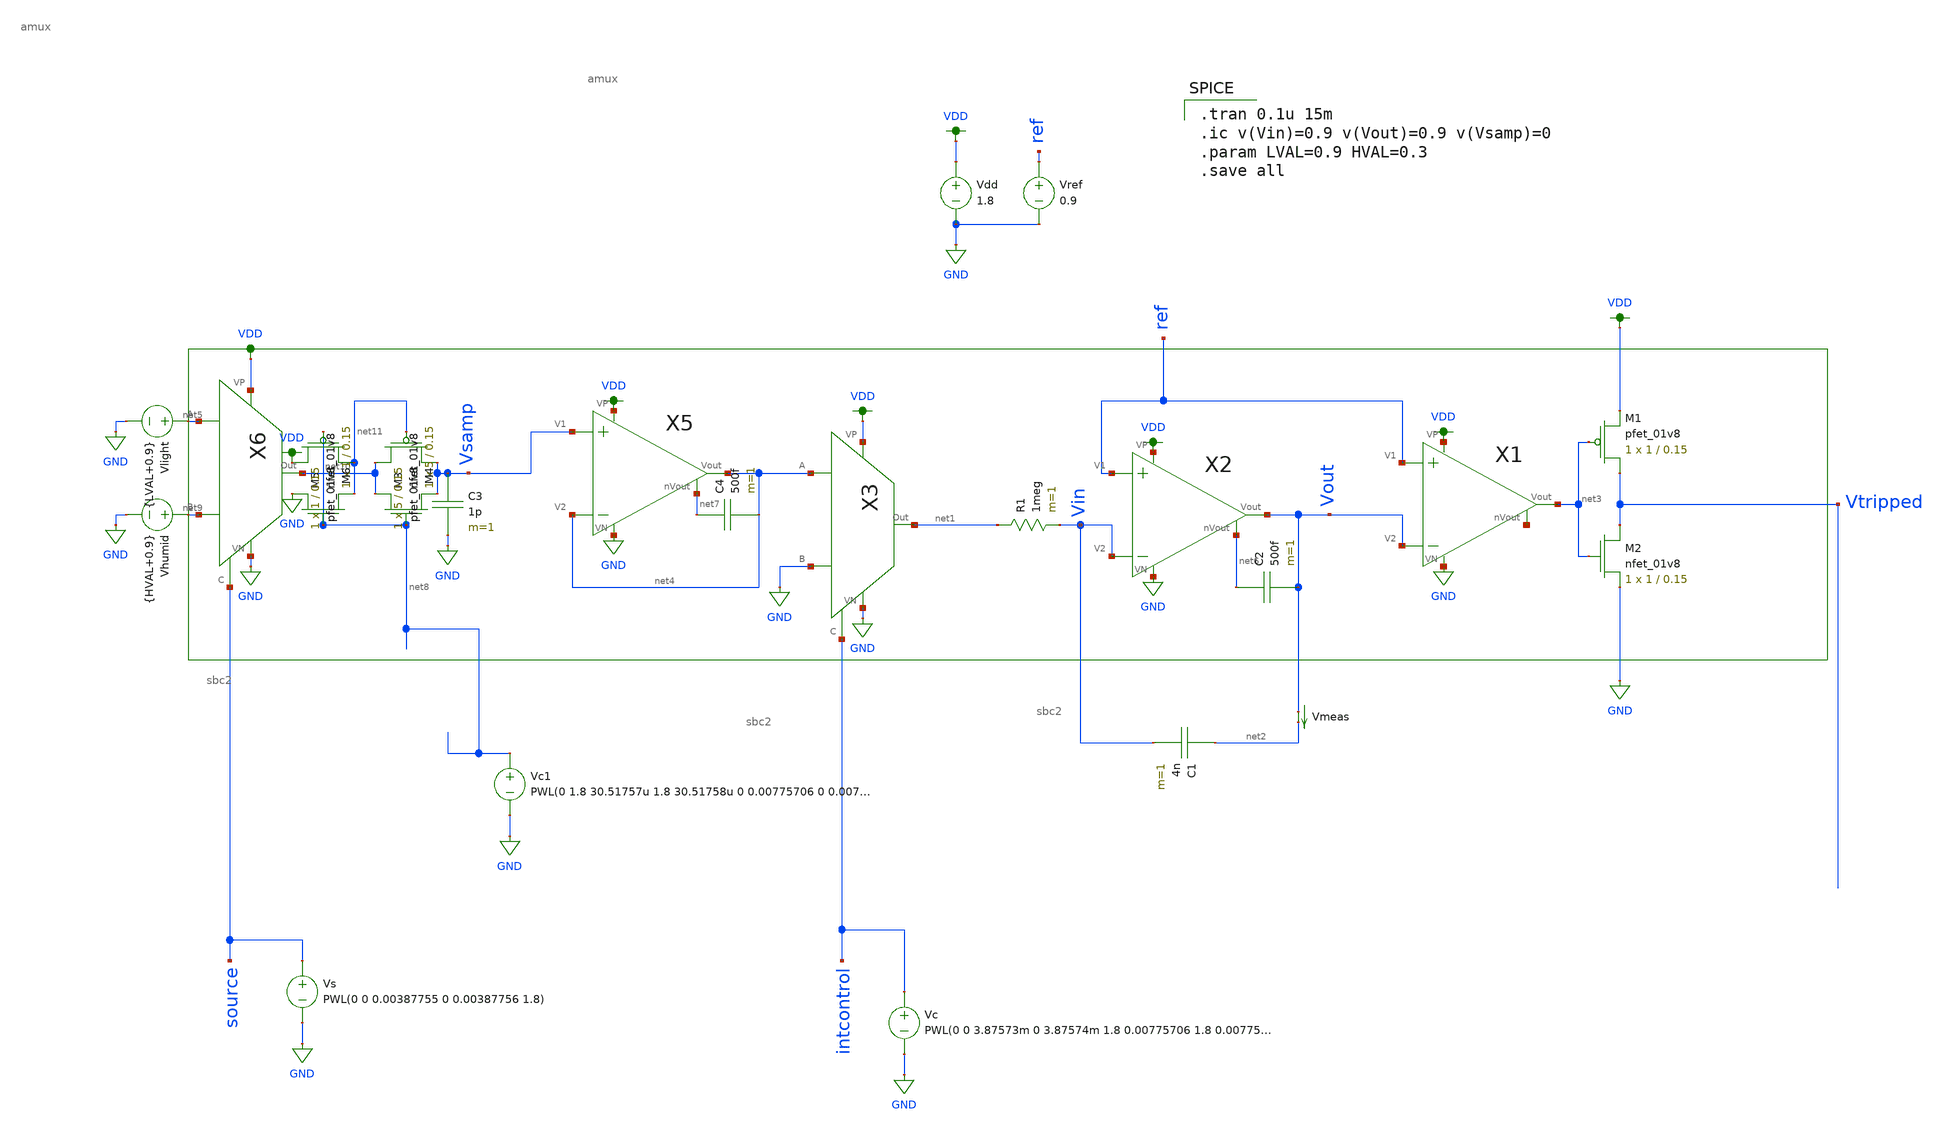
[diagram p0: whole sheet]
** sch_path: analog/adc_testing.sch
**.subckt adc_testing
Vdd VDD GND 1.8
C1 net2 Vin 4n m=1
R1 net1 Vin 1meg m=1
Vlight net5 GND {LVAL+0.9}
Vref ref GND 0.9
Vmeas Vout net2 0
.save i(vmeas)
XM1 Vtripped net3 VDD VDD sky130_fd_pr__pfet_01v8 L=0.15 W=1 nf=1 ad='int((nf+1)/2) * W/nf * 0.29' as='int((nf+2)/2) * W/nf * 0.29'
+ pd='2*int((nf+1)/2) * (W/nf + 0.29)' ps='2*int((nf+2)/2) * (W/nf + 0.29)' nrd='0.29 / W' nrs='0.29 / W'
+ sa=0 sb=0 sd=0 mult=1 m=1
XM2 Vtripped net3 GND GND sky130_fd_pr__nfet_01v8 L=0.15 W=1 nf=1 ad='int((nf+1)/2) * W/nf * 0.29' as='int((nf+2)/2) * W/nf * 0.29'
+ pd='2*int((nf+1)/2) * (W/nf + 0.29)' ps='2*int((nf+2)/2) * (W/nf + 0.29)' nrd='0.29 / W' nrs='0.29 / W'
+ sa=0 sb=0 sd=0 mult=1 m=1
X3 net4 GND net1 VDD GND intcontrol amux
C2 net6 Vout 500f m=1
X1 ref Vout net12 net3 GND VDD sbc2
X2 ref Vin net6 Vout GND VDD sbc2
X5 Vsamp net4 net7 net4 GND VDD sbc2
C3 Vsamp GND 1p m=1
C4 net7 net4 500f m=1
XM3 net10 net8 Vsamp GND sky130_fd_pr__nfet_01v8 L=0.15 W=5 nf=1 ad='int((nf+1)/2) * W/nf * 0.29' as='int((nf+2)/2) * W/nf * 0.29'
+ pd='2*int((nf+1)/2) * (W/nf + 0.29)' ps='2*int((nf+2)/2) * (W/nf + 0.29)' nrd='0.29 / W' nrs='0.29 / W'
+ sa=0 sb=0 sd=0 mult=1 m=1
X6 net5 net9 net10 VDD GND source amux
Vhumid net9 GND {HVAL+0.9}
Vs source GND PWL(0 0 0.00387755 0 0.00387756 1.8)
Vc intcontrol GND PWL(0 0 3.87573m 0 3.87574m 1.8 0.00775706 1.8 0.007757061 0 0.01163461 0
+ 0.01163462 1.8)
XM4 net10 net11 Vsamp VDD sky130_fd_pr__pfet_01v8 L=0.15 W=5 nf=1 ad='int((nf+1)/2) * W/nf * 0.29' as='int((nf+2)/2) * W/nf * 0.29'
+ pd='2*int((nf+1)/2) * (W/nf + 0.29)' ps='2*int((nf+2)/2) * (W/nf + 0.29)' nrd='0.29 / W' nrs='0.29 / W'
+ sa=0 sb=0 sd=0 mult=1 m=1
Vc1 net8 GND PWL(0 1.8 30.51757u 1.8 30.51758u 0 0.00775706 0 0.007757061 1.8 0.00778757 1.8
+ 0.00778758 0)
XM5 GND net8 net11 GND sky130_fd_pr__nfet_01v8 L=0.15 W=1 nf=1 ad='int((nf+1)/2) * W/nf * 0.29' as='int((nf+2)/2) * W/nf * 0.29'
+ pd='2*int((nf+1)/2) * (W/nf + 0.29)' ps='2*int((nf+2)/2) * (W/nf + 0.29)' nrd='0.29 / W' nrs='0.29 / W'
+ sa=0 sb=0 sd=0 mult=1 m=1
XM6 VDD net8 net11 VDD sky130_fd_pr__pfet_01v8 L=0.15 W=1 nf=1 ad='int((nf+1)/2) * W/nf * 0.29' as='int((nf+2)/2) * W/nf * 0.29'
+ pd='2*int((nf+1)/2) * (W/nf + 0.29)' ps='2*int((nf+2)/2) * (W/nf + 0.29)' nrd='0.29 / W' nrs='0.29 / W'
+ sa=0 sb=0 sd=0 mult=1 m=1
**** begin user architecture code

.option wnflag=1
.param MC_SWITCH=0.0
.lib ~/skywater/skywater-pdk/libraries/sky130_fd_pr_ngspice/latest/models/sky130.lib.spice tt


.tran 0.1u 15m
.ic v(Vin)=0.9 v(Vout)=0.9 v(Vsamp)=0
.param LVAL=0.9 HVAL=0.3
.save all

**** end user architecture code
**.ends

* expanding   symbol:  /home/jonah/VLSI/final/amux.sym # of pins=6
** sym_path: analog/amux.sym
** sch_path: analog/amux.sch
.subckt amux A B Out VP VN C
*.iopin VN
*.iopin VP
*.ipin C
*.ipin A
*.ipin B
*.opin Out
XM1 B net1 Out VDD sky130_fd_pr__pfet_01v8 L=0.15 W=1 nf=1 ad='int((nf+1)/2) * W/nf * 0.29' as='int((nf+2)/2) * W/nf * 0.29'
+ pd='2*int((nf+1)/2) * (W/nf + 0.29)' ps='2*int((nf+2)/2) * (W/nf + 0.29)' nrd='0.29 / W' nrs='0.29 / W'
+ sa=0 sb=0 sd=0 mult=1 m=1
XM2 Out C B GND sky130_fd_pr__nfet_01v8 L=0.15 W=1 nf=1 ad='int((nf+1)/2) * W/nf * 0.29' as='int((nf+2)/2) * W/nf * 0.29'
+ pd='2*int((nf+1)/2) * (W/nf + 0.29)' ps='2*int((nf+2)/2) * (W/nf + 0.29)' nrd='0.29 / W' nrs='0.29 / W'
+ sa=0 sb=0 sd=0 mult=1 m=1
XM3 Out C A VDD sky130_fd_pr__pfet_01v8 L=0.15 W=1 nf=1 ad='int((nf+1)/2) * W/nf * 0.29' as='int((nf+2)/2) * W/nf * 0.29'
+ pd='2*int((nf+1)/2) * (W/nf + 0.29)' ps='2*int((nf+2)/2) * (W/nf + 0.29)' nrd='0.29 / W' nrs='0.29 / W'
+ sa=0 sb=0 sd=0 mult=1 m=1
XM4 A net1 Out GND sky130_fd_pr__nfet_01v8 L=0.15 W=1 nf=1 ad='int((nf+1)/2) * W/nf * 0.29' as='int((nf+2)/2) * W/nf * 0.29'
+ pd='2*int((nf+1)/2) * (W/nf + 0.29)' ps='2*int((nf+2)/2) * (W/nf + 0.29)' nrd='0.29 / W' nrs='0.29 / W'
+ sa=0 sb=0 sd=0 mult=1 m=1
XM5 net1 C VP VDD sky130_fd_pr__pfet_01v8 L=0.15 W=1 nf=1 ad='int((nf+1)/2) * W/nf * 0.29' as='int((nf+2)/2) * W/nf * 0.29'
+ pd='2*int((nf+1)/2) * (W/nf + 0.29)' ps='2*int((nf+2)/2) * (W/nf + 0.29)' nrd='0.29 / W' nrs='0.29 / W'
+ sa=0 sb=0 sd=0 mult=1 m=1
XM6 VN C net1 GND sky130_fd_pr__nfet_01v8 L=0.15 W=1 nf=1 ad='int((nf+1)/2) * W/nf * 0.29' as='int((nf+2)/2) * W/nf * 0.29'
+ pd='2*int((nf+1)/2) * (W/nf + 0.29)' ps='2*int((nf+2)/2) * (W/nf + 0.29)' nrd='0.29 / W' nrs='0.29 / W'
+ sa=0 sb=0 sd=0 mult=1 m=1
.ends


* expanding   symbol:  /home/jonah/VLSI/final/sbc2.sym # of pins=6
** sym_path: analog/sbc2.sym
** sch_path: analog/sbc2.sch
.subckt sbc2 V1 V2 nVout Vout VN VP
*.ipin V1
*.ipin V2
*.iopin Vout
*.iopin nVout
*.iopin VP
*.iopin VN
XM7a net2 V1 net1 GND sky130_fd_pr__nfet_01v8 L=0.6 W=1.5 nf=1 ad='int((nf+1)/2) * W/nf * 0.29' as='int((nf+2)/2) * W/nf * 0.29'
+ pd='2*int((nf+1)/2) * (W/nf + 0.29)' ps='2*int((nf+2)/2) * (W/nf + 0.29)' nrd='0.29 / W' nrs='0.29 / W'
+ sa=0 sb=0 sd=0 mult=1 m=1
XM8a net3 V2 net2 GND sky130_fd_pr__nfet_01v8 L=0.6 W=1.5 nf=1 ad='int((nf+1)/2) * W/nf * 0.29' as='int((nf+2)/2) * W/nf * 0.29'
+ pd='2*int((nf+1)/2) * (W/nf + 0.29)' ps='2*int((nf+2)/2) * (W/nf + 0.29)' nrd='0.29 / W' nrs='0.29 / W'
+ sa=0 sb=0 sd=0 mult=1 m=1
XM8b net2 V2 net3 GND sky130_fd_pr__nfet_01v8 L=0.6 W=1.5 nf=1 ad='int((nf+1)/2) * W/nf * 0.29' as='int((nf+2)/2) * W/nf * 0.29'
+ pd='2*int((nf+1)/2) * (W/nf + 0.29)' ps='2*int((nf+2)/2) * (W/nf + 0.29)' nrd='0.29 / W' nrs='0.29 / W'
+ sa=0 sb=0 sd=0 mult=1 m=1
XM7b net1 V1 net2 GND sky130_fd_pr__nfet_01v8 L=0.6 W=1.5 nf=1 ad='int((nf+1)/2) * W/nf * 0.29' as='int((nf+2)/2) * W/nf * 0.29'
+ pd='2*int((nf+1)/2) * (W/nf + 0.29)' ps='2*int((nf+2)/2) * (W/nf + 0.29)' nrd='0.29 / W' nrs='0.29 / W'
+ sa=0 sb=0 sd=0 mult=1 m=1
XMd1 net1 VN VN GND sky130_fd_pr__nfet_01v8 L=0.6 W=1.5 nf=1 ad='int((nf+1)/2) * W/nf * 0.29' as='int((nf+2)/2) * W/nf * 0.29'
+ pd='2*int((nf+1)/2) * (W/nf + 0.29)' ps='2*int((nf+2)/2) * (W/nf + 0.29)' nrd='0.29 / W' nrs='0.29 / W'
+ sa=0 sb=0 sd=0 mult=1 m=1
XMd2 VN VN net1 GND sky130_fd_pr__nfet_01v8 L=0.6 W=1.5 nf=1 ad='int((nf+1)/2) * W/nf * 0.29' as='int((nf+2)/2) * W/nf * 0.29'
+ pd='2*int((nf+1)/2) * (W/nf + 0.29)' ps='2*int((nf+2)/2) * (W/nf + 0.29)' nrd='0.29 / W' nrs='0.29 / W'
+ sa=0 sb=0 sd=0 mult=1 m=1
XMd3 VP VP net4 VDD sky130_fd_pr__pfet_01v8 L=0.6 W=1.5 nf=1 ad='int((nf+1)/2) * W/nf * 0.29' as='int((nf+2)/2) * W/nf * 0.29'
+ pd='2*int((nf+1)/2) * (W/nf + 0.29)' ps='2*int((nf+2)/2) * (W/nf + 0.29)' nrd='0.29 / W' nrs='0.29 / W'
+ sa=0 sb=0 sd=0 mult=1 m=1
XM15a net4 V2 net5 VDD sky130_fd_pr__pfet_01v8 L=0.6 W=1.5 nf=1 ad='int((nf+1)/2) * W/nf * 0.29' as='int((nf+2)/2) * W/nf * 0.29'
+ pd='2*int((nf+1)/2) * (W/nf + 0.29)' ps='2*int((nf+2)/2) * (W/nf + 0.29)' nrd='0.29 / W' nrs='0.29 / W'
+ sa=0 sb=0 sd=0 mult=1 m=1
XM16a net5 V1 net6 VDD sky130_fd_pr__pfet_01v8 L=0.6 W=1.5 nf=1 ad='int((nf+1)/2) * W/nf * 0.29' as='int((nf+2)/2) * W/nf * 0.29'
+ pd='2*int((nf+1)/2) * (W/nf + 0.29)' ps='2*int((nf+2)/2) * (W/nf + 0.29)' nrd='0.29 / W' nrs='0.29 / W'
+ sa=0 sb=0 sd=0 mult=1 m=1
XM16b net6 V1 net5 VDD sky130_fd_pr__pfet_01v8 L=0.6 W=1.5 nf=1 ad='int((nf+1)/2) * W/nf * 0.29' as='int((nf+2)/2) * W/nf * 0.29'
+ pd='2*int((nf+1)/2) * (W/nf + 0.29)' ps='2*int((nf+2)/2) * (W/nf + 0.29)' nrd='0.29 / W' nrs='0.29 / W'
+ sa=0 sb=0 sd=0 mult=1 m=1
XM15b net5 V2 net4 VDD sky130_fd_pr__pfet_01v8 L=0.6 W=1.5 nf=1 ad='int((nf+1)/2) * W/nf * 0.29' as='int((nf+2)/2) * W/nf * 0.29'
+ pd='2*int((nf+1)/2) * (W/nf + 0.29)' ps='2*int((nf+2)/2) * (W/nf + 0.29)' nrd='0.29 / W' nrs='0.29 / W'
+ sa=0 sb=0 sd=0 mult=1 m=1
XMd4 net4 VP VP VDD sky130_fd_pr__pfet_01v8 L=0.6 W=1.5 nf=1 ad='int((nf+1)/2) * W/nf * 0.29' as='int((nf+2)/2) * W/nf * 0.29'
+ pd='2*int((nf+1)/2) * (W/nf + 0.29)' ps='2*int((nf+2)/2) * (W/nf + 0.29)' nrd='0.29 / W' nrs='0.29 / W'
+ sa=0 sb=0 sd=0 mult=1 m=1
XM20a net8 net9 net7 VDD sky130_fd_pr__pfet_01v8 L=0.6 W=1.5 nf=1 ad='int((nf+1)/2) * W/nf * 0.29' as='int((nf+2)/2) * W/nf * 0.29'
+ pd='2*int((nf+1)/2) * (W/nf + 0.29)' ps='2*int((nf+2)/2) * (W/nf + 0.29)' nrd='0.29 / W' nrs='0.29 / W'
+ sa=0 sb=0 sd=0 mult=1 m=1
XM21a net7 net9 VP VDD sky130_fd_pr__pfet_01v8 L=0.6 W=1.5 nf=1 ad='int((nf+1)/2) * W/nf * 0.29' as='int((nf+2)/2) * W/nf * 0.29'
+ pd='2*int((nf+1)/2) * (W/nf + 0.29)' ps='2*int((nf+2)/2) * (W/nf + 0.29)' nrd='0.29 / W' nrs='0.29 / W'
+ sa=0 sb=0 sd=0 mult=1 m=1
XM14a VP net9 net6 VDD sky130_fd_pr__pfet_01v8 L=0.6 W=1.5 nf=1 ad='int((nf+1)/2) * W/nf * 0.29' as='int((nf+2)/2) * W/nf * 0.29'
+ pd='2*int((nf+1)/2) * (W/nf + 0.29)' ps='2*int((nf+2)/2) * (W/nf + 0.29)' nrd='0.29 / W' nrs='0.29 / W'
+ sa=0 sb=0 sd=0 mult=1 m=1
XM14b net6 net9 VP VDD sky130_fd_pr__pfet_01v8 L=0.6 W=1.5 nf=1 ad='int((nf+1)/2) * W/nf * 0.29' as='int((nf+2)/2) * W/nf * 0.29'
+ pd='2*int((nf+1)/2) * (W/nf + 0.29)' ps='2*int((nf+2)/2) * (W/nf + 0.29)' nrd='0.29 / W' nrs='0.29 / W'
+ sa=0 sb=0 sd=0 mult=1 m=1
XM21b VP net9 net7 VDD sky130_fd_pr__pfet_01v8 L=0.6 W=1.5 nf=1 ad='int((nf+1)/2) * W/nf * 0.29' as='int((nf+2)/2) * W/nf * 0.29'
+ pd='2*int((nf+1)/2) * (W/nf + 0.29)' ps='2*int((nf+2)/2) * (W/nf + 0.29)' nrd='0.29 / W' nrs='0.29 / W'
+ sa=0 sb=0 sd=0 mult=1 m=1
XM20b net7 net9 net8 VDD sky130_fd_pr__pfet_01v8 L=0.6 W=1.5 nf=1 ad='int((nf+1)/2) * W/nf * 0.29' as='int((nf+2)/2) * W/nf * 0.29'
+ pd='2*int((nf+1)/2) * (W/nf + 0.29)' ps='2*int((nf+2)/2) * (W/nf + 0.29)' nrd='0.29 / W' nrs='0.29 / W'
+ sa=0 sb=0 sd=0 mult=1 m=1
XMd5 net8 VP VP VDD sky130_fd_pr__pfet_01v8 L=0.6 W=1.5 nf=1 ad='int((nf+1)/2) * W/nf * 0.29' as='int((nf+2)/2) * W/nf * 0.29'
+ pd='2*int((nf+1)/2) * (W/nf + 0.29)' ps='2*int((nf+2)/2) * (W/nf + 0.29)' nrd='0.29 / W' nrs='0.29 / W'
+ sa=0 sb=0 sd=0 mult=1 m=1
XMd6 VP VP net8 VDD sky130_fd_pr__pfet_01v8 L=0.6 W=1.5 nf=1 ad='int((nf+1)/2) * W/nf * 0.29' as='int((nf+2)/2) * W/nf * 0.29'
+ pd='2*int((nf+1)/2) * (W/nf + 0.29)' ps='2*int((nf+2)/2) * (W/nf + 0.29)' nrd='0.29 / W' nrs='0.29 / W'
+ sa=0 sb=0 sd=0 mult=1 m=1
XM22a VN net9 net7 VDD sky130_fd_pr__pfet_01v8 L=0.6 W=1.5 nf=1 ad='int((nf+1)/2) * W/nf * 0.29' as='int((nf+2)/2) * W/nf * 0.29'
+ pd='2*int((nf+1)/2) * (W/nf + 0.29)' ps='2*int((nf+2)/2) * (W/nf + 0.29)' nrd='0.29 / W' nrs='0.29 / W'
+ sa=0 sb=0 sd=0 mult=1 m=1
XM22b net7 net9 VN VDD sky130_fd_pr__pfet_01v8 L=0.6 W=1.5 nf=1 ad='int((nf+1)/2) * W/nf * 0.29' as='int((nf+2)/2) * W/nf * 0.29'
+ pd='2*int((nf+1)/2) * (W/nf + 0.29)' ps='2*int((nf+2)/2) * (W/nf + 0.29)' nrd='0.29 / W' nrs='0.29 / W'
+ sa=0 sb=0 sd=0 mult=1 m=1
XM22c VN net9 net7 VDD sky130_fd_pr__pfet_01v8 L=0.6 W=1.5 nf=1 ad='int((nf+1)/2) * W/nf * 0.29' as='int((nf+2)/2) * W/nf * 0.29'
+ pd='2*int((nf+1)/2) * (W/nf + 0.29)' ps='2*int((nf+2)/2) * (W/nf + 0.29)' nrd='0.29 / W' nrs='0.29 / W'
+ sa=0 sb=0 sd=0 mult=1 m=1
XM22d net7 net9 VN VDD sky130_fd_pr__pfet_01v8 L=0.6 W=1.5 nf=1 ad='int((nf+1)/2) * W/nf * 0.29' as='int((nf+2)/2) * W/nf * 0.29'
+ pd='2*int((nf+1)/2) * (W/nf + 0.29)' ps='2*int((nf+2)/2) * (W/nf + 0.29)' nrd='0.29 / W' nrs='0.29 / W'
+ sa=0 sb=0 sd=0 mult=1 m=1
XM22e VN net9 net7 VDD sky130_fd_pr__pfet_01v8 L=0.6 W=1.5 nf=1 ad='int((nf+1)/2) * W/nf * 0.29' as='int((nf+2)/2) * W/nf * 0.29'
+ pd='2*int((nf+1)/2) * (W/nf + 0.29)' ps='2*int((nf+2)/2) * (W/nf + 0.29)' nrd='0.29 / W' nrs='0.29 / W'
+ sa=0 sb=0 sd=0 mult=1 m=1
XM22f net7 net9 VN VDD sky130_fd_pr__pfet_01v8 L=0.6 W=1.5 nf=1 ad='int((nf+1)/2) * W/nf * 0.29' as='int((nf+2)/2) * W/nf * 0.29'
+ pd='2*int((nf+1)/2) * (W/nf + 0.29)' ps='2*int((nf+2)/2) * (W/nf + 0.29)' nrd='0.29 / W' nrs='0.29 / W'
+ sa=0 sb=0 sd=0 mult=1 m=1
XMd7 VN VP VP VDD sky130_fd_pr__pfet_01v8 L=0.6 W=1.5 nf=1 ad='int((nf+1)/2) * W/nf * 0.29' as='int((nf+2)/2) * W/nf * 0.29'
+ pd='2*int((nf+1)/2) * (W/nf + 0.29)' ps='2*int((nf+2)/2) * (W/nf + 0.29)' nrd='0.29 / W' nrs='0.29 / W'
+ sa=0 sb=0 sd=0 mult=1 m=1
XMd8 VP VP VN VDD sky130_fd_pr__pfet_01v8 L=0.6 W=1.5 nf=1 ad='int((nf+1)/2) * W/nf * 0.29' as='int((nf+2)/2) * W/nf * 0.29'
+ pd='2*int((nf+1)/2) * (W/nf + 0.29)' ps='2*int((nf+2)/2) * (W/nf + 0.29)' nrd='0.29 / W' nrs='0.29 / W'
+ sa=0 sb=0 sd=0 mult=1 m=1
XM18a net10 net8 net9 GND sky130_fd_pr__nfet_01v8 L=0.6 W=1.5 nf=1 ad='int((nf+1)/2) * W/nf * 0.29' as='int((nf+2)/2) * W/nf * 0.29'
+ pd='2*int((nf+1)/2) * (W/nf + 0.29)' ps='2*int((nf+2)/2) * (W/nf + 0.29)' nrd='0.29 / W' nrs='0.29 / W'
+ sa=0 sb=0 sd=0 mult=1 m=1
XM17a VN net8 net10 GND sky130_fd_pr__nfet_01v8 L=0.6 W=1.5 nf=1 ad='int((nf+1)/2) * W/nf * 0.29' as='int((nf+2)/2) * W/nf * 0.29'
+ pd='2*int((nf+1)/2) * (W/nf + 0.29)' ps='2*int((nf+2)/2) * (W/nf + 0.29)' nrd='0.29 / W' nrs='0.29 / W'
+ sa=0 sb=0 sd=0 mult=1 m=1
XM6a net2 net8 VN GND sky130_fd_pr__nfet_01v8 L=0.6 W=1.5 nf=1 ad='int((nf+1)/2) * W/nf * 0.29' as='int((nf+2)/2) * W/nf * 0.29'
+ pd='2*int((nf+1)/2) * (W/nf + 0.29)' ps='2*int((nf+2)/2) * (W/nf + 0.29)' nrd='0.29 / W' nrs='0.29 / W'
+ sa=0 sb=0 sd=0 mult=1 m=1
XM6b VN net8 net2 GND sky130_fd_pr__nfet_01v8 L=0.6 W=1.5 nf=1 ad='int((nf+1)/2) * W/nf * 0.29' as='int((nf+2)/2) * W/nf * 0.29'
+ pd='2*int((nf+1)/2) * (W/nf + 0.29)' ps='2*int((nf+2)/2) * (W/nf + 0.29)' nrd='0.29 / W' nrs='0.29 / W'
+ sa=0 sb=0 sd=0 mult=1 m=1
XMd9 net9 VN VN GND sky130_fd_pr__nfet_01v8 L=0.6 W=1.5 nf=1 ad='int((nf+1)/2) * W/nf * 0.29' as='int((nf+2)/2) * W/nf * 0.29'
+ pd='2*int((nf+1)/2) * (W/nf + 0.29)' ps='2*int((nf+2)/2) * (W/nf + 0.29)' nrd='0.29 / W' nrs='0.29 / W'
+ sa=0 sb=0 sd=0 mult=1 m=1
XM17b net10 net8 VN GND sky130_fd_pr__nfet_01v8 L=0.6 W=1.5 nf=1 ad='int((nf+1)/2) * W/nf * 0.29' as='int((nf+2)/2) * W/nf * 0.29'
+ pd='2*int((nf+1)/2) * (W/nf + 0.29)' ps='2*int((nf+2)/2) * (W/nf + 0.29)' nrd='0.29 / W' nrs='0.29 / W'
+ sa=0 sb=0 sd=0 mult=1 m=1
XM18b net9 net8 net10 GND sky130_fd_pr__nfet_01v8 L=0.6 W=1.5 nf=1 ad='int((nf+1)/2) * W/nf * 0.29' as='int((nf+2)/2) * W/nf * 0.29'
+ pd='2*int((nf+1)/2) * (W/nf + 0.29)' ps='2*int((nf+2)/2) * (W/nf + 0.29)' nrd='0.29 / W' nrs='0.29 / W'
+ sa=0 sb=0 sd=0 mult=1 m=1
XMd10 VN VN net9 GND sky130_fd_pr__nfet_01v8 L=0.6 W=1.5 nf=1 ad='int((nf+1)/2) * W/nf * 0.29' as='int((nf+2)/2) * W/nf * 0.29'
+ pd='2*int((nf+1)/2) * (W/nf + 0.29)' ps='2*int((nf+2)/2) * (W/nf + 0.29)' nrd='0.29 / W' nrs='0.29 / W'
+ sa=0 sb=0 sd=0 mult=1 m=1
XM19a net10 net8 VP GND sky130_fd_pr__nfet_01v8 L=0.6 W=1.5 nf=1 ad='int((nf+1)/2) * W/nf * 0.29' as='int((nf+2)/2) * W/nf * 0.29'
+ pd='2*int((nf+1)/2) * (W/nf + 0.29)' ps='2*int((nf+2)/2) * (W/nf + 0.29)' nrd='0.29 / W' nrs='0.29 / W'
+ sa=0 sb=0 sd=0 mult=1 m=1
XM19b VP net8 net10 GND sky130_fd_pr__nfet_01v8 L=0.6 W=1.5 nf=1 ad='int((nf+1)/2) * W/nf * 0.29' as='int((nf+2)/2) * W/nf * 0.29'
+ pd='2*int((nf+1)/2) * (W/nf + 0.29)' ps='2*int((nf+2)/2) * (W/nf + 0.29)' nrd='0.29 / W' nrs='0.29 / W'
+ sa=0 sb=0 sd=0 mult=1 m=1
XM19c net10 net8 VP GND sky130_fd_pr__nfet_01v8 L=0.6 W=1.5 nf=1 ad='int((nf+1)/2) * W/nf * 0.29' as='int((nf+2)/2) * W/nf * 0.29'
+ pd='2*int((nf+1)/2) * (W/nf + 0.29)' ps='2*int((nf+2)/2) * (W/nf + 0.29)' nrd='0.29 / W' nrs='0.29 / W'
+ sa=0 sb=0 sd=0 mult=1 m=1
XM19d VP net8 net10 GND sky130_fd_pr__nfet_01v8 L=0.6 W=1.5 nf=1 ad='int((nf+1)/2) * W/nf * 0.29' as='int((nf+2)/2) * W/nf * 0.29'
+ pd='2*int((nf+1)/2) * (W/nf + 0.29)' ps='2*int((nf+2)/2) * (W/nf + 0.29)' nrd='0.29 / W' nrs='0.29 / W'
+ sa=0 sb=0 sd=0 mult=1 m=1
XMd11 VP VN VN GND sky130_fd_pr__nfet_01v8 L=0.6 W=1.5 nf=1 ad='int((nf+1)/2) * W/nf * 0.29' as='int((nf+2)/2) * W/nf * 0.29'
+ pd='2*int((nf+1)/2) * (W/nf + 0.29)' ps='2*int((nf+2)/2) * (W/nf + 0.29)' nrd='0.29 / W' nrs='0.29 / W'
+ sa=0 sb=0 sd=0 mult=1 m=1
XM19e net10 net8 VP GND sky130_fd_pr__nfet_01v8 L=0.6 W=1.5 nf=1 ad='int((nf+1)/2) * W/nf * 0.29' as='int((nf+2)/2) * W/nf * 0.29'
+ pd='2*int((nf+1)/2) * (W/nf + 0.29)' ps='2*int((nf+2)/2) * (W/nf + 0.29)' nrd='0.29 / W' nrs='0.29 / W'
+ sa=0 sb=0 sd=0 mult=1 m=1
XM19f VP net8 net10 GND sky130_fd_pr__nfet_01v8 L=0.6 W=1.5 nf=1 ad='int((nf+1)/2) * W/nf * 0.29' as='int((nf+2)/2) * W/nf * 0.29'
+ pd='2*int((nf+1)/2) * (W/nf + 0.29)' ps='2*int((nf+2)/2) * (W/nf + 0.29)' nrd='0.29 / W' nrs='0.29 / W'
+ sa=0 sb=0 sd=0 mult=1 m=1
XMd14 VN VN VP GND sky130_fd_pr__nfet_01v8 L=0.6 W=1.5 nf=1 ad='int((nf+1)/2) * W/nf * 0.29' as='int((nf+2)/2) * W/nf * 0.29'
+ pd='2*int((nf+1)/2) * (W/nf + 0.29)' ps='2*int((nf+2)/2) * (W/nf + 0.29)' nrd='0.29 / W' nrs='0.29 / W'
+ sa=0 sb=0 sd=0 mult=1 m=1
XM13a net3 net9 net9 VDD sky130_fd_pr__pfet_01v8 L=0.6 W=1.5 nf=1 ad='int((nf+1)/2) * W/nf * 0.29' as='int((nf+2)/2) * W/nf * 0.29'
+ pd='2*int((nf+1)/2) * (W/nf + 0.29)' ps='2*int((nf+2)/2) * (W/nf + 0.29)' nrd='0.29 / W' nrs='0.29 / W'
+ sa=0 sb=0 sd=0 mult=1 m=1
XM13b net9 net9 net3 VDD sky130_fd_pr__pfet_01v8 L=0.6 W=1.5 nf=1 ad='int((nf+1)/2) * W/nf * 0.29' as='int((nf+2)/2) * W/nf * 0.29'
+ pd='2*int((nf+1)/2) * (W/nf + 0.29)' ps='2*int((nf+2)/2) * (W/nf + 0.29)' nrd='0.29 / W' nrs='0.29 / W'
+ sa=0 sb=0 sd=0 mult=1 m=1
XM10a net3 net9 VP VDD sky130_fd_pr__pfet_01v8 L=0.6 W=1.5 nf=1 ad='int((nf+1)/2) * W/nf * 0.29' as='int((nf+2)/2) * W/nf * 0.29'
+ pd='2*int((nf+1)/2) * (W/nf + 0.29)' ps='2*int((nf+2)/2) * (W/nf + 0.29)' nrd='0.29 / W' nrs='0.29 / W'
+ sa=0 sb=0 sd=0 mult=1 m=1
XM9a VP net9 net1 VDD sky130_fd_pr__pfet_01v8 L=0.6 W=1.5 nf=1 ad='int((nf+1)/2) * W/nf * 0.29' as='int((nf+2)/2) * W/nf * 0.29'
+ pd='2*int((nf+1)/2) * (W/nf + 0.29)' ps='2*int((nf+2)/2) * (W/nf + 0.29)' nrd='0.29 / W' nrs='0.29 / W'
+ sa=0 sb=0 sd=0 mult=1 m=1
XM9b net1 net9 VP VDD sky130_fd_pr__pfet_01v8 L=0.6 W=1.5 nf=1 ad='int((nf+1)/2) * W/nf * 0.29' as='int((nf+2)/2) * W/nf * 0.29'
+ pd='2*int((nf+1)/2) * (W/nf + 0.29)' ps='2*int((nf+2)/2) * (W/nf + 0.29)' nrd='0.29 / W' nrs='0.29 / W'
+ sa=0 sb=0 sd=0 mult=1 m=1
XM10b VP net9 net3 VDD sky130_fd_pr__pfet_01v8 L=0.6 W=1.5 nf=1 ad='int((nf+1)/2) * W/nf * 0.29' as='int((nf+2)/2) * W/nf * 0.29'
+ pd='2*int((nf+1)/2) * (W/nf + 0.29)' ps='2*int((nf+2)/2) * (W/nf + 0.29)' nrd='0.29 / W' nrs='0.29 / W'
+ sa=0 sb=0 sd=0 mult=1 m=1
XMd12 VP VP net3 VDD sky130_fd_pr__pfet_01v8 L=0.6 W=1.5 nf=1 ad='int((nf+1)/2) * W/nf * 0.29' as='int((nf+2)/2) * W/nf * 0.29'
+ pd='2*int((nf+1)/2) * (W/nf + 0.29)' ps='2*int((nf+2)/2) * (W/nf + 0.29)' nrd='0.29 / W' nrs='0.29 / W'
+ sa=0 sb=0 sd=0 mult=1 m=1
XMd13 net3 VP VP VDD sky130_fd_pr__pfet_01v8 L=0.6 W=1.5 nf=1 ad='int((nf+1)/2) * W/nf * 0.29' as='int((nf+2)/2) * W/nf * 0.29'
+ pd='2*int((nf+1)/2) * (W/nf + 0.29)' ps='2*int((nf+2)/2) * (W/nf + 0.29)' nrd='0.29 / W' nrs='0.29 / W'
+ sa=0 sb=0 sd=0 mult=1 m=1
XM5a net8 net8 net4 GND sky130_fd_pr__nfet_01v8 L=0.6 W=1.5 nf=1 ad='int((nf+1)/2) * W/nf * 0.29' as='int((nf+2)/2) * W/nf * 0.29'
+ pd='2*int((nf+1)/2) * (W/nf + 0.29)' ps='2*int((nf+2)/2) * (W/nf + 0.29)' nrd='0.29 / W' nrs='0.29 / W'
+ sa=0 sb=0 sd=0 mult=1 m=1
XM5b net4 net8 net8 GND sky130_fd_pr__nfet_01v8 L=0.6 W=1.5 nf=1 ad='int((nf+1)/2) * W/nf * 0.29' as='int((nf+2)/2) * W/nf * 0.29'
+ pd='2*int((nf+1)/2) * (W/nf + 0.29)' ps='2*int((nf+2)/2) * (W/nf + 0.29)' nrd='0.29 / W' nrs='0.29 / W'
+ sa=0 sb=0 sd=0 mult=1 m=1
XM2a VN net8 net4 GND sky130_fd_pr__nfet_01v8 L=0.6 W=1.5 nf=1 ad='int((nf+1)/2) * W/nf * 0.29' as='int((nf+2)/2) * W/nf * 0.29'
+ pd='2*int((nf+1)/2) * (W/nf + 0.29)' ps='2*int((nf+2)/2) * (W/nf + 0.29)' nrd='0.29 / W' nrs='0.29 / W'
+ sa=0 sb=0 sd=0 mult=1 m=1
XM1a net5 net8 VN GND sky130_fd_pr__nfet_01v8 L=0.6 W=1.5 nf=1 ad='int((nf+1)/2) * W/nf * 0.29' as='int((nf+2)/2) * W/nf * 0.29'
+ pd='2*int((nf+1)/2) * (W/nf + 0.29)' ps='2*int((nf+2)/2) * (W/nf + 0.29)' nrd='0.29 / W' nrs='0.29 / W'
+ sa=0 sb=0 sd=0 mult=1 m=1
XMd15 net4 VN VN GND sky130_fd_pr__nfet_01v8 L=0.6 W=1.5 nf=1 ad='int((nf+1)/2) * W/nf * 0.29' as='int((nf+2)/2) * W/nf * 0.29'
+ pd='2*int((nf+1)/2) * (W/nf + 0.29)' ps='2*int((nf+2)/2) * (W/nf + 0.29)' nrd='0.29 / W' nrs='0.29 / W'
+ sa=0 sb=0 sd=0 mult=1 m=1
XM1b VN net8 net5 GND sky130_fd_pr__nfet_01v8 L=0.6 W=1.5 nf=1 ad='int((nf+1)/2) * W/nf * 0.29' as='int((nf+2)/2) * W/nf * 0.29'
+ pd='2*int((nf+1)/2) * (W/nf + 0.29)' ps='2*int((nf+2)/2) * (W/nf + 0.29)' nrd='0.29 / W' nrs='0.29 / W'
+ sa=0 sb=0 sd=0 mult=1 m=1
XM2b net4 net8 VN GND sky130_fd_pr__nfet_01v8 L=0.6 W=1.5 nf=1 ad='int((nf+1)/2) * W/nf * 0.29' as='int((nf+2)/2) * W/nf * 0.29'
+ pd='2*int((nf+1)/2) * (W/nf + 0.29)' ps='2*int((nf+2)/2) * (W/nf + 0.29)' nrd='0.29 / W' nrs='0.29 / W'
+ sa=0 sb=0 sd=0 mult=1 m=1
XMd18 VN VN net4 GND sky130_fd_pr__nfet_01v8 L=0.6 W=1.5 nf=1 ad='int((nf+1)/2) * W/nf * 0.29' as='int((nf+2)/2) * W/nf * 0.29'
+ pd='2*int((nf+1)/2) * (W/nf + 0.29)' ps='2*int((nf+2)/2) * (W/nf + 0.29)' nrd='0.29 / W' nrs='0.29 / W'
+ sa=0 sb=0 sd=0 mult=1 m=1
XM12a net3 net11 net11 VDD sky130_fd_pr__pfet_01v8 L=0.6 W=1.5 nf=1 ad='int((nf+1)/2) * W/nf * 0.29'
+ as='int((nf+2)/2) * W/nf * 0.29' pd='2*int((nf+1)/2) * (W/nf + 0.29)' ps='2*int((nf+2)/2) * (W/nf + 0.29)'
+ nrd='0.29 / W' nrs='0.29 / W' sa=0 sb=0 sd=0 mult=1 m=1
XM11a nVout net11 net1 VDD sky130_fd_pr__pfet_01v8 L=0.6 W=1.5 nf=1 ad='int((nf+1)/2) * W/nf * 0.29'
+ as='int((nf+2)/2) * W/nf * 0.29' pd='2*int((nf+1)/2) * (W/nf + 0.29)' ps='2*int((nf+2)/2) * (W/nf + 0.29)'
+ nrd='0.29 / W' nrs='0.29 / W' sa=0 sb=0 sd=0 mult=1 m=1
XM11b net1 net11 nVout VDD sky130_fd_pr__pfet_01v8 L=0.6 W=1.5 nf=1 ad='int((nf+1)/2) * W/nf * 0.29'
+ as='int((nf+2)/2) * W/nf * 0.29' pd='2*int((nf+1)/2) * (W/nf + 0.29)' ps='2*int((nf+2)/2) * (W/nf + 0.29)'
+ nrd='0.29 / W' nrs='0.29 / W' sa=0 sb=0 sd=0 mult=1 m=1
XM12b net11 net11 net3 VDD sky130_fd_pr__pfet_01v8 L=0.6 W=1.5 nf=1 ad='int((nf+1)/2) * W/nf * 0.29'
+ as='int((nf+2)/2) * W/nf * 0.29' pd='2*int((nf+1)/2) * (W/nf + 0.29)' ps='2*int((nf+2)/2) * (W/nf + 0.29)'
+ nrd='0.29 / W' nrs='0.29 / W' sa=0 sb=0 sd=0 mult=1 m=1
XMd16 net3 VP VP VDD sky130_fd_pr__pfet_01v8 L=0.6 W=1.5 nf=1 ad='int((nf+1)/2) * W/nf * 0.29' as='int((nf+2)/2) * W/nf * 0.29'
+ pd='2*int((nf+1)/2) * (W/nf + 0.29)' ps='2*int((nf+2)/2) * (W/nf + 0.29)' nrd='0.29 / W' nrs='0.29 / W'
+ sa=0 sb=0 sd=0 mult=1 m=1
XMd17 VP VP net3 VDD sky130_fd_pr__pfet_01v8 L=0.6 W=1.5 nf=1 ad='int((nf+1)/2) * W/nf * 0.29' as='int((nf+2)/2) * W/nf * 0.29'
+ pd='2*int((nf+1)/2) * (W/nf + 0.29)' ps='2*int((nf+2)/2) * (W/nf + 0.29)' nrd='0.29 / W' nrs='0.29 / W'
+ sa=0 sb=0 sd=0 mult=1 m=1
XM3a net5 net11 nVout GND sky130_fd_pr__nfet_01v8 L=0.6 W=1.5 nf=1 ad='int((nf+1)/2) * W/nf * 0.29' as='int((nf+2)/2) * W/nf * 0.29'
+ pd='2*int((nf+1)/2) * (W/nf + 0.29)' ps='2*int((nf+2)/2) * (W/nf + 0.29)' nrd='0.29 / W' nrs='0.29 / W'
+ sa=0 sb=0 sd=0 mult=1 m=1
XM4a net11 net11 net4 GND sky130_fd_pr__nfet_01v8 L=0.6 W=1.5 nf=1 ad='int((nf+1)/2) * W/nf * 0.29' as='int((nf+2)/2) * W/nf * 0.29'
+ pd='2*int((nf+1)/2) * (W/nf + 0.29)' ps='2*int((nf+2)/2) * (W/nf + 0.29)' nrd='0.29 / W' nrs='0.29 / W'
+ sa=0 sb=0 sd=0 mult=1 m=1
XM3b nVout net11 net5 GND sky130_fd_pr__nfet_01v8 L=0.6 W=1.5 nf=1 ad='int((nf+1)/2) * W/nf * 0.29' as='int((nf+2)/2) * W/nf * 0.29'
+ pd='2*int((nf+1)/2) * (W/nf + 0.29)' ps='2*int((nf+2)/2) * (W/nf + 0.29)' nrd='0.29 / W' nrs='0.29 / W'
+ sa=0 sb=0 sd=0 mult=1 m=1
XM4b net4 net11 net11 GND sky130_fd_pr__nfet_01v8 L=0.6 W=1.5 nf=1 ad='int((nf+1)/2) * W/nf * 0.29' as='int((nf+2)/2) * W/nf * 0.29'
+ pd='2*int((nf+1)/2) * (W/nf + 0.29)' ps='2*int((nf+2)/2) * (W/nf + 0.29)' nrd='0.29 / W' nrs='0.29 / W'
+ sa=0 sb=0 sd=0 mult=1 m=1
XMd19 VN VN net4 GND sky130_fd_pr__nfet_01v8 L=0.6 W=1.5 nf=1 ad='int((nf+1)/2) * W/nf * 0.29' as='int((nf+2)/2) * W/nf * 0.29'
+ pd='2*int((nf+1)/2) * (W/nf + 0.29)' ps='2*int((nf+2)/2) * (W/nf + 0.29)' nrd='0.29 / W' nrs='0.29 / W'
+ sa=0 sb=0 sd=0 mult=1 m=1
XMd20 net4 VN VN GND sky130_fd_pr__nfet_01v8 L=0.6 W=1.5 nf=1 ad='int((nf+1)/2) * W/nf * 0.29' as='int((nf+2)/2) * W/nf * 0.29'
+ pd='2*int((nf+1)/2) * (W/nf + 0.29)' ps='2*int((nf+2)/2) * (W/nf + 0.29)' nrd='0.29 / W' nrs='0.29 / W'
+ sa=0 sb=0 sd=0 mult=1 m=1
XM2 Vout nVout VN GND sky130_fd_pr__nfet_01v8 L=0.15 W=6 nf=1 ad='int((nf+1)/2) * W/nf * 0.29' as='int((nf+2)/2) * W/nf * 0.29'
+ pd='2*int((nf+1)/2) * (W/nf + 0.29)' ps='2*int((nf+2)/2) * (W/nf + 0.29)' nrd='0.29 / W' nrs='0.29 / W'
+ sa=0 sb=0 sd=0 mult=1 m=1
XM23 VP nVout Vout VDD sky130_fd_pr__pfet_01v8 L=0.15 W=12 nf=1 ad='int((nf+1)/2) * W/nf * 0.29' as='int((nf+2)/2) * W/nf * 0.29'
+ pd='2*int((nf+1)/2) * (W/nf + 0.29)' ps='2*int((nf+2)/2) * (W/nf + 0.29)' nrd='0.29 / W' nrs='0.29 / W'
+ sa=0 sb=0 sd=0 mult=1 m=1
.ends

.GLOBAL VDD
.GLOBAL GND
.end
